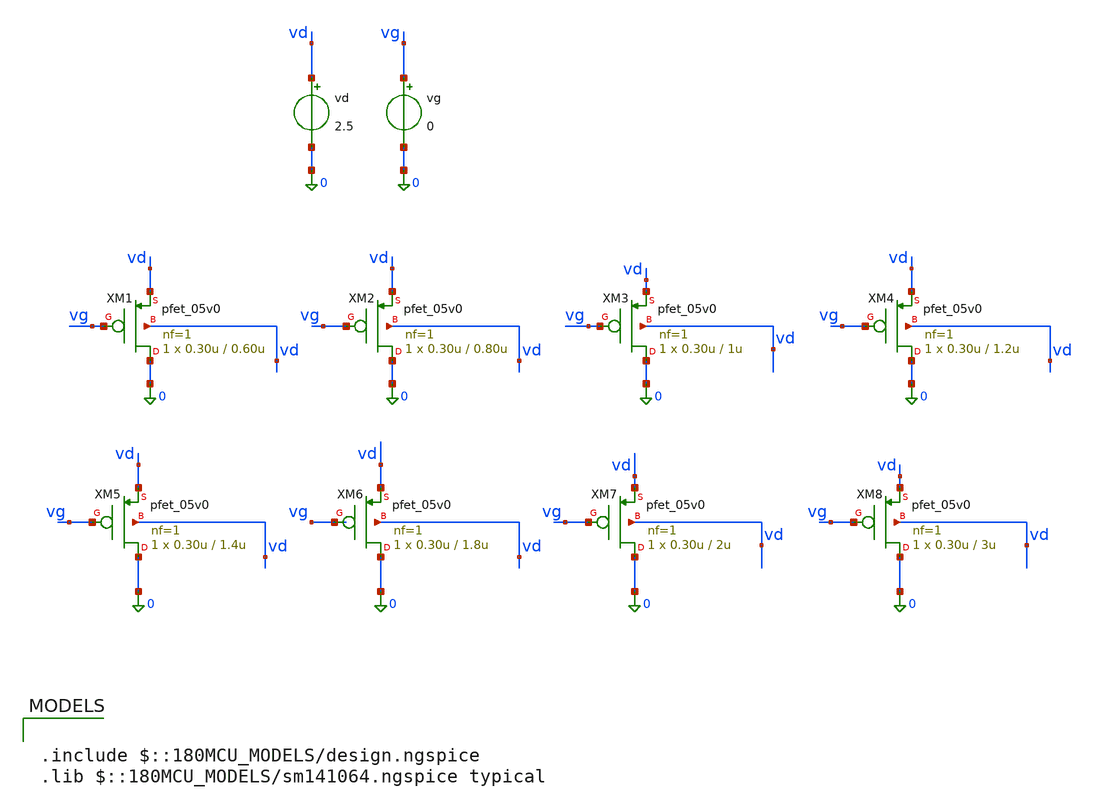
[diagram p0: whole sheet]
** sch_path: Gm_ID Design Charts (GF 180 MCU) For BGR/Schematic/Gm_ID_gf180mcu_PMOS.sch
**.subckt Gm_ID_gf180mcu_PMOS
vd vd 0 2.5
vg vg 0 0
XM8 0 vg vd vd pfet_05v0 L=3u W=0.30u nf=1 ad='int((nf+1)/2) * W/nf * 0.18u' as='int((nf+2)/2) * W/nf * 0.18u'
+ pd='2*int((nf+1)/2) * (W/nf + 0.18u)' ps='2*int((nf+2)/2) * (W/nf + 0.18u)' nrd='0.18u / W' nrs='0.18u / W'
+ sa=0 sb=0 sd=0 m=1
XM1 0 vg vd vd pfet_05v0 L=0.60u W=0.30u nf=1 ad='int((nf+1)/2) * W/nf * 0.18u' as='int((nf+2)/2) * W/nf * 0.18u'
+ pd='2*int((nf+1)/2) * (W/nf + 0.18u)' ps='2*int((nf+2)/2) * (W/nf + 0.18u)' nrd='0.18u / W' nrs='0.18u / W'
+ sa=0 sb=0 sd=0 m=1
XM2 0 vg vd vd pfet_05v0 L=0.80u W=0.30u nf=1 ad='int((nf+1)/2) * W/nf * 0.18u' as='int((nf+2)/2) * W/nf * 0.18u'
+ pd='2*int((nf+1)/2) * (W/nf + 0.18u)' ps='2*int((nf+2)/2) * (W/nf + 0.18u)' nrd='0.18u / W' nrs='0.18u / W'
+ sa=0 sb=0 sd=0 m=1
XM3 0 vg vd vd pfet_05v0 L=1u W=0.30u nf=1 ad='int((nf+1)/2) * W/nf * 0.18u' as='int((nf+2)/2) * W/nf * 0.18u'
+ pd='2*int((nf+1)/2) * (W/nf + 0.18u)' ps='2*int((nf+2)/2) * (W/nf + 0.18u)' nrd='0.18u / W' nrs='0.18u / W'
+ sa=0 sb=0 sd=0 m=1
XM4 0 vg vd vd pfet_05v0 L=1.2u W=0.30u nf=1 ad='int((nf+1)/2) * W/nf * 0.18u' as='int((nf+2)/2) * W/nf * 0.18u'
+ pd='2*int((nf+1)/2) * (W/nf + 0.18u)' ps='2*int((nf+2)/2) * (W/nf + 0.18u)' nrd='0.18u / W' nrs='0.18u / W'
+ sa=0 sb=0 sd=0 m=1
XM5 0 vg vd vd pfet_05v0 L=1.4u W=0.30u nf=1 ad='int((nf+1)/2) * W/nf * 0.18u' as='int((nf+2)/2) * W/nf * 0.18u'
+ pd='2*int((nf+1)/2) * (W/nf + 0.18u)' ps='2*int((nf+2)/2) * (W/nf + 0.18u)' nrd='0.18u / W' nrs='0.18u / W'
+ sa=0 sb=0 sd=0 m=1
XM6 0 vg vd vd pfet_05v0 L=1.8u W=0.30u nf=1 ad='int((nf+1)/2) * W/nf * 0.18u' as='int((nf+2)/2) * W/nf * 0.18u'
+ pd='2*int((nf+1)/2) * (W/nf + 0.18u)' ps='2*int((nf+2)/2) * (W/nf + 0.18u)' nrd='0.18u / W' nrs='0.18u / W'
+ sa=0 sb=0 sd=0 m=1
XM7 0 vg vd vd pfet_05v0 L=2u W=0.30u nf=1 ad='int((nf+1)/2) * W/nf * 0.18u' as='int((nf+2)/2) * W/nf * 0.18u'
+ pd='2*int((nf+1)/2) * (W/nf + 0.18u)' ps='2*int((nf+2)/2) * (W/nf + 0.18u)' nrd='0.18u / W' nrs='0.18u / W'
+ sa=0 sb=0 sd=0 m=1
**** begin user architecture code

.include $::180MCU_MODELS/design.ngspice
.lib $::180MCU_MODELS/sm141064.ngspice typical



.option wnflag=1
.option savecurrents
.control

save @m.xm1.m0[gm]
save @m.xm1.m0[vth]
save @m.xm1.m0[gds]
save @m.xm1.m0[id]
save @m.xm1.m0[vds]
save @m.xm1.m0[cgg]
save @m.xm1.m0[vgs]

save @m.xm2.m0[gm]
save @m.xm2.m0[vth]
save @m.xm2.m0[gds]
save @m.xm2.m0[id]
save @m.xm2.m0[vds]
save @m.xm2.m0[cgg]
save @m.xm2.m0[vgs]

save @m.xm3.m0[gm]
save @m.xm3.m0[vth]
save @m.xm3.m0[gds]
save @m.xm3.m0[id]
save @m.xm3.m0[vds]
save @m.xm3.m0[cgg]
save @m.xm3.m0[vgs]

save @m.xm4.m0[gm]
save @m.xm4.m0[vth]
save @m.xm4.m0[gds]
save @m.xm4.m0[id]
save @m.xm4.m0[vds]
save @m.xm4.m0[cgg]
save @m.xm4.m0[vgs]

save @m.xm5.m0[gm]
save @m.xm5.m0[vth]
save @m.xm5.m0[gds]
save @m.xm5.m0[id]
save @m.xm5.m0[vds]
save @m.xm5.m0[cgg]
save @m.xm5.m0[vgs]

save @m.xm6.m0[gm]
save @m.xm6.m0[vth]
save @m.xm6.m0[gds]
save @m.xm6.m0[id]
save @m.xm6.m0[vds]
save @m.xm6.m0[cgg]
save @m.xm6.m0[vgs]

save @m.xm7.m0[gm]
save @m.xm7.m0[vth]
save @m.xm7.m0[gds]
save @m.xm7.m0[id]
save @m.xm7.m0[vds]
save @m.xm7.m0[cgg]
save @m.xm7.m0[vgs]

save @m.xm8.m0[gm]
save @m.xm8.m0[vth]
save @m.xm8.m0[gds]
save @m.xm8.m0[id]
save @m.xm8.m0[vds]
save @m.xm8.m0[cgg]
save @m.xm8.m0[vgs]

dc VG 0.05 0.10 0.01
remzerovec

write gf180_pmos_5V.raw

wrdata gmid_gf180_pmos51.txt  @m.xm1.m0[gm]  @m.xm1.m0[gds]  @m.xm1.m0[id]  @m.xm1.m0[w]
+  @m.xm1.m0[vds]  @m.xm1.m0[cgg]  @m.xm1.m0[vgs]  @m.xm1.m0[vth]

wrdata gmid_gf180_pmos52.txt  @m.xm2.m0[gm]  @m.xm2.m0[gds]  @m.xm2.m0[id]  @m.xm2.m0[w]
+  @m.xm2.m0[vds]  @m.xm2.m0[cgg]  @m.xm2.m0[vgs]  @m.xm2.m0[vth]

wrdata gmid_gf180_pmos53.txt  @m.xm3.m0[gm]  @m.xm3.m0[gds]  @m.xm3.m0[id]  @m.xm3.m0[w]
+  @m.xm3.m0[vds]  @m.xm3.m0[cgg]  @m.xm3.m0[vgs]  @m.xm3.m0[vth]

wrdata gmid_gf180_pmos54.txt  @m.xm4.m0[gm]  @m.xm4.m0[gds]  @m.xm4.m0[id]  @m.xm4.m0[w]
+  @m.xm4.m0[vds]  @m.xm4.m0[cgg]  @m.xm4.m0[vgs]  @m.xm4.m0[vth]

wrdata gmid_gf180_pmos55.txt  @m.xm5.m0[gm]  @m.xm5.m0[gds]  @m.xm5.m0[id]  @m.xm5.m0[w]
+  @m.xm5.m0[vds]  @m.xm5.m0[cgg]  @m.xm5.m0[vgs]  @m.xm5.m0[vth]

wrdata gmid_gf180_pmos56.txt  @m.xm6.m0[gm]  @m.xm6.m0[gds]  @m.xm6.m0[id]  @m.xm6.m0[w]
+  @m.xm6.m0[vds]  @m.xm6.m0[cgg]  @m.xm6.m0[vgs]  @m.xm6.m0[vth]

wrdata gmid_gf180_pmos57.txt  @m.xm7.m0[gm]  @m.xm7.m0[gds]  @m.xm7.m0[id]  @m.xm7.m0[w]
+  @m.xm7.m0[vds]  @m.xm7.m0[cgg]  @m.xm7.m0[vgs]  @m.xm7.m0[vth]

wrdata gmid_gf180_pmos58.txt  @m.xm8.m0[gm]  @m.xm8.m0[gds]  @m.xm8.m0[id]  @m.xm8.m0[w]
+  @m.xm8.m0[vds]  @m.xm8.m0[cgg]  @m.xm8.m0[vgs]  @m.xm8.m0[vth]

print @m.xm1.m0[gm]
print @m.xm1.m0[id]
print @m.xm1.m0[cgg]
print @m.xm1.m0[qg]


remzerovec
.endc


**** end user architecture code
**.ends
.end
